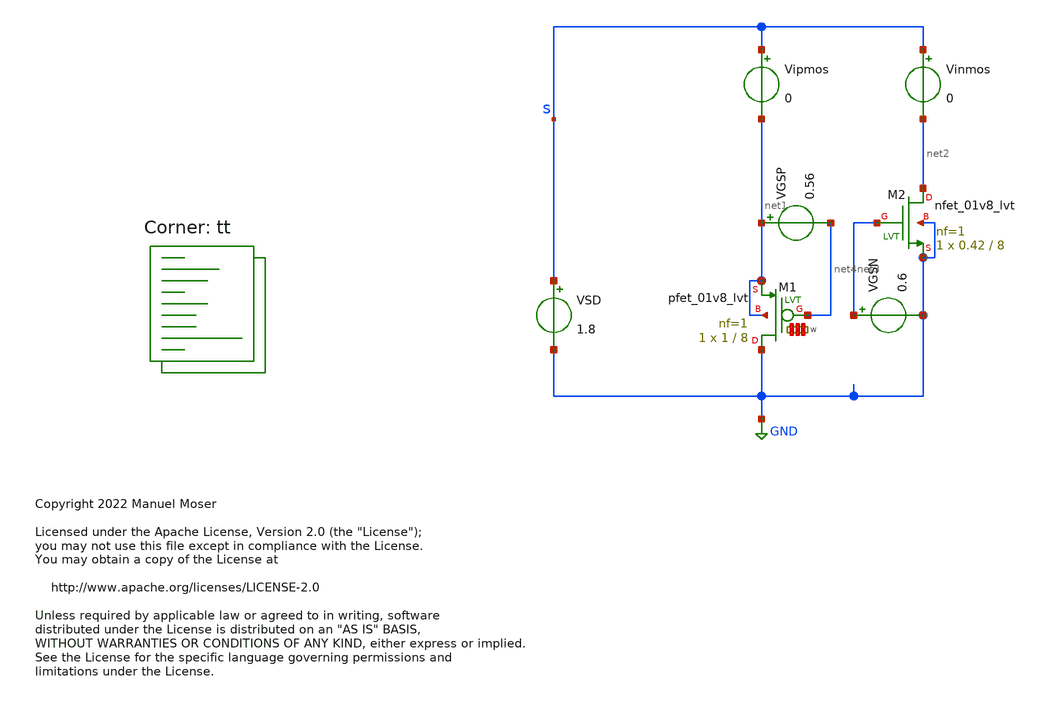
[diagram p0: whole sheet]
** sch_path: xschem/archive/transistor_size_tb.sch
* Copyright 2022 Manuel Moser
* Licensed under the Apache License, Version 2.0 (the "License");
**.subckt transistor_size_tb
XM1 GND net4 net1 net1 sky130_fd_pr__pfet_01v8_lvt L=8 W='1 * 1 ' nf=1 ad='int((nf+1)/2) * W / nf * 0.29'
+ as='int((nf+2)/2) * W / nf * 0.29' pd='2*int((nf+1)/2) * (W / nf + 0.29)' ps='2*int((nf+2)/2) * (W / nf + 0.29)'
+ nrd='0.29 / W ' nrs='0.29 / W ' sa=0 sb=0 sd=0 mult=1 m=1
VSD s GND 1.8
XM2 net2 net3 GND GND sky130_fd_pr__nfet_01v8_lvt L=8 W=0.42 nf=1 ad='int((nf+1)/2) * W/nf * 0.29' as='int((nf+2)/2) * W/nf * 0.29'
+ pd='2*int((nf+1)/2) * (W/nf + 0.29)' ps='2*int((nf+2)/2) * (W/nf + 0.29)' nrd='0.29 / W' nrs='0.29 / W'
+ sa=0 sb=0 sd=0 mult=1 m=1
VGSP net1 net4 0.56
VGSN net3 GND 0.6
Vipmos s net1 0
Vinmos s net2 0
**** begin user architecture code



.temp 27

.save all
.save @m.xm1.msky130_fd_pr__pfet_01v8_lvt[Vth]
.save @m.xm2.msky130_fd_pr__nfet_01v8_lvt[Vth]

.control
set num_threads=12
dc VSD 0 1.8 0.1
plot (i(vipmos))
plot (i(vinmos))

op
write pmos_power_transistor_tb.raw
print v(@m.xm1.msky130_fd_pr__pfet_01v8_lvt[Vth])
print v(@m.xm2.msky130_fd_pr__nfet_01v8_lvt[Vth])

.endc



.lib $::SKYWATER_MODELS/sky130.lib.spice tt
**** end user architecture code
**.ends
.GLOBAL GND
.end
